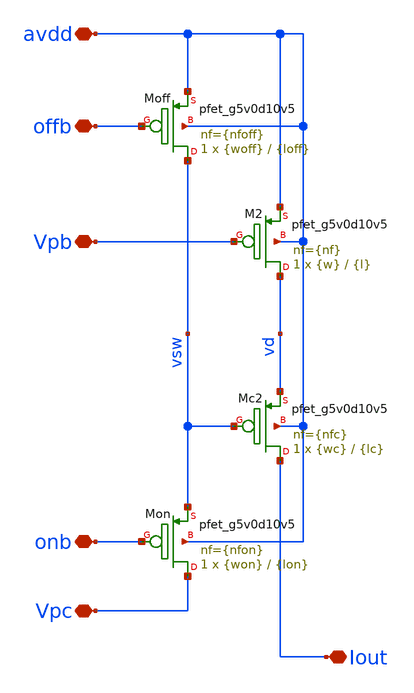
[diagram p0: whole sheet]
** sch_path: xschem/sky130_cm_sw_psource.sch
**.subckt sky130_cm_sw_psource avdd Vpb Vpc Iout offb onb
*.iopin avdd
*.iopin Vpb
*.iopin Vpc
*.iopin Iout
*.iopin offb
*.iopin onb
XMc2 Iout vsw vd avdd sky130_fd_pr__pfet_g5v0d10v5 L={lc} W={wc} nf={nfc} ad='int(({nfc} + 1)/2) * {wc} / {nfc} * 0.29'
+ as='int(({nfc} + 2)/2) * {wc} / {nfc} * 0.29' pd='2*int(({nfc} + 1)/2) * ({wc} / {nfc} + 0.29)' ps='2*int(({nfc} + 2)/2) * ({wc} / {nfc} + 0.29)'
+ nrd='0.29 / {wc} ' nrs='0.29 / {wc} ' sa=0 sb=0 sd=0 mult=1 m=1
XM2 vd Vpb avdd avdd sky130_fd_pr__pfet_g5v0d10v5 L={l} W={w} nf={nf} ad='int(({nf} + 1)/2) * {w} / {nf} * 0.29'
+ as='int(({nf} + 2)/2) * {w} / {nf} * 0.29' pd='2*int(({nf} + 1)/2) * ({w} / {nf} + 0.29)' ps='2*int(({nf} + 2)/2) * ({w} / {nf} + 0.29)'
+ nrd='0.29 / {w} ' nrs='0.29 / {w} ' sa=0 sb=0 sd=0 mult=1 m=1
XMon Vpc onb vsw avdd sky130_fd_pr__pfet_g5v0d10v5 L={lon} W={won} nf={nfon} ad='int(({nfon} + 1)/2) * {won} / {nfon} * 0.29'
+ as='int(({nfon} + 2)/2) * {won} / {nfon} * 0.29' pd='2*int(({nfon} + 1)/2) * ({won} / {nfon} + 0.29)'
+ ps='2*int(({nfon} + 2)/2) * ({won} / {nfon} + 0.29)' nrd='0.29 / {won} ' nrs='0.29 / {won} ' sa=0 sb=0
+ sd=0 mult=1 m=1
XMoff vsw offb avdd avdd sky130_fd_pr__pfet_g5v0d10v5 L={loff} W={woff} nf={nfoff} ad='int(({nfoff} + 1)/2) * {woff} / {nfoff} * 0.29'
+ as='int(({nfoff} + 2)/2) * {woff} / {nfoff} * 0.29' pd='2*int(({nfoff} + 1)/2) * ({woff} / {nfoff} + 0.29)'
+ ps='2*int(({nfoff} + 2)/2) * ({woff} / {nfoff} + 0.29)' nrd='0.29 / {woff} ' nrs='0.29 / {woff} ' sa=0
+ sb=0 sd=0 mult=1 m=1
**.ends
.end
